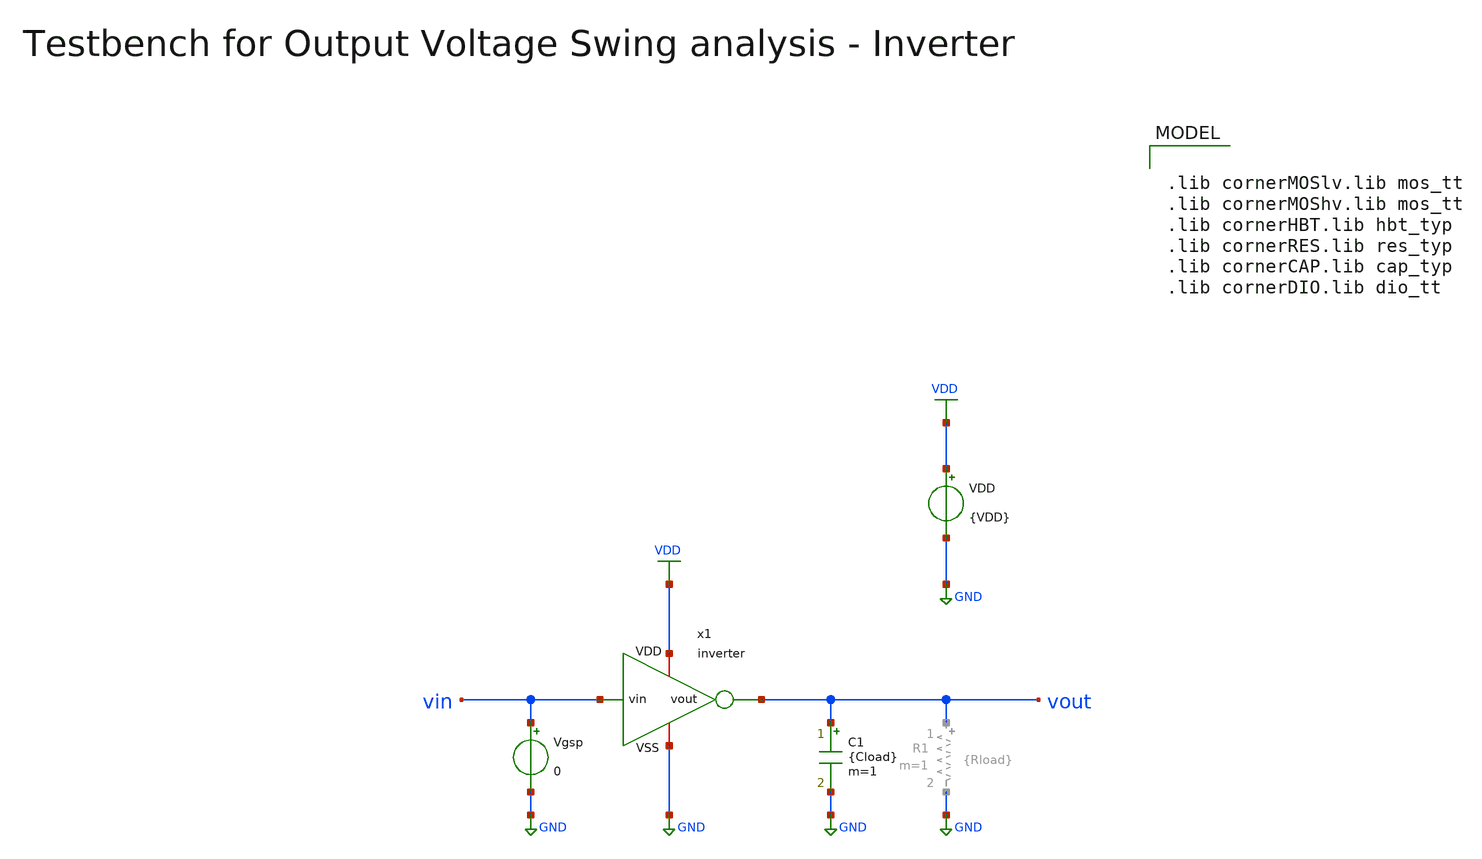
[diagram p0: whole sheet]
** sch_path: macros/inverter/testbenches/inverter_tb_Vout.sch
**.subckt inverter_tb_Vout
VDD VDD GND {VDD}
C1 vout GND {Cload} m=1
Vgsp vin GND 0
x1 VDD vin vout GND inverter
**** begin user architecture code


* .include ../../netlist/pex/inverter_top_pex.spice
.param VDD=1.5
.csparam VDD=VDD
.param Vcm=VDD/2
.csparam Vcm=Vcm
.param temp=27
.param Cload=10p
.param Rload=1k
.options savecurrents klu method=gear reltol=1e-3 abstol=1e-15 gmin=1e-15
.control

save all

* Operating Point Analysis
op
remzerovec
write @schname\.raw
set appendwrite

* DC Sweep
dc Vgsp 0 $&VDD 1m
remzerovec
write @schname\.raw
set appendwrite

* Plotting
plot vin vout

* Measurement
meas dc Vgsp_at_Vcm when vout=Vcm
print Vgsp_at_Vcm

* Write Data
unset appendwrite
set wr_vecnames
set wr_singlescale
wrdata $PROJECT_PATH/scripts/plot_simulations/data/inverter_top_tb_Vout.txt v(vin) v(vout)

*quit
.endc



.lib cornerMOSlv.lib mos_tt
.lib cornerMOShv.lib mos_tt
.lib cornerHBT.lib hbt_typ
.lib cornerRES.lib res_typ
.lib cornerCAP.lib cap_typ
.lib cornerDIO.lib dio_tt

**** end user architecture code
**.ends
.GLOBAL GND
.GLOBAL VDD
.end
